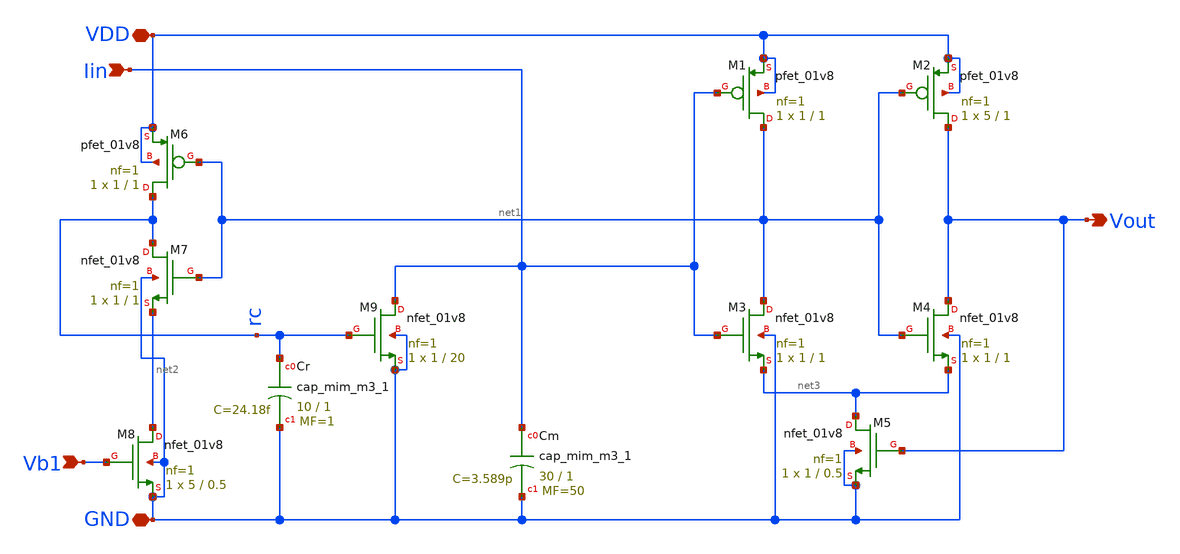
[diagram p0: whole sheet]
** sch_path: LIF_neuron/LIF_neuron_Vohra_CC.sch
**.subckt LIF_neuron_Vohra_CC GND Vb1 VDD Vout Iin
*.iopin GND
*.ipin Vb1
*.iopin VDD
*.opin Vout
*.ipin Iin
XM8 net2 Vb1 GND GND sky130_fd_pr__nfet_01v8 L=0.5 W=5 nf=1 ad='int((nf+1)/2) * W/nf * 0.29' as='int((nf+2)/2) * W/nf * 0.29'
+ pd='2*int((nf+1)/2) * (W/nf + 0.29)' ps='2*int((nf+2)/2) * (W/nf + 0.29)' nrd='0.29 / W' nrs='0.29 / W'
+ sa=0 sb=0 sd=0 mult=1 m=1
XM7 rc net1 net2 GND sky130_fd_pr__nfet_01v8 L=1 W=1 nf=1 ad='int((nf+1)/2) * W/nf * 0.29' as='int((nf+2)/2) * W/nf * 0.29'
+ pd='2*int((nf+1)/2) * (W/nf + 0.29)' ps='2*int((nf+2)/2) * (W/nf + 0.29)' nrd='0.29 / W' nrs='0.29 / W'
+ sa=0 sb=0 sd=0 mult=1 m=1
XM6 rc net1 VDD VDD sky130_fd_pr__pfet_01v8 L=1 W=1 nf=1 ad='int((nf+1)/2) * W/nf * 0.29' as='int((nf+2)/2) * W/nf * 0.29'
+ pd='2*int((nf+1)/2) * (W/nf + 0.29)' ps='2*int((nf+2)/2) * (W/nf + 0.29)' nrd='0.29 / W' nrs='0.29 / W'
+ sa=0 sb=0 sd=0 mult=1 m=1
XCr rc GND sky130_fd_pr__cap_mim_m3_1 W=10 L=1 MF=1 m=1
XM9 Iin rc GND GND sky130_fd_pr__nfet_01v8 L=20 W=1 nf=1 ad='int((nf+1)/2) * W/nf * 0.29' as='int((nf+2)/2) * W/nf * 0.29'
+ pd='2*int((nf+1)/2) * (W/nf + 0.29)' ps='2*int((nf+2)/2) * (W/nf + 0.29)' nrd='0.29 / W' nrs='0.29 / W'
+ sa=0 sb=0 sd=0 mult=1 m=1
XCm Iin GND sky130_fd_pr__cap_mim_m3_1 W=30 L=1 MF=50 m=50
XM5 net3 Vout GND GND sky130_fd_pr__nfet_01v8 L=0.5 W=1 nf=1 ad='int((nf+1)/2) * W/nf * 0.29' as='int((nf+2)/2) * W/nf * 0.29'
+ pd='2*int((nf+1)/2) * (W/nf + 0.29)' ps='2*int((nf+2)/2) * (W/nf + 0.29)' nrd='0.29 / W' nrs='0.29 / W'
+ sa=0 sb=0 sd=0 mult=1 m=1
XM3 net1 Iin net3 GND sky130_fd_pr__nfet_01v8 L=1 W=1 nf=1 ad='int((nf+1)/2) * W/nf * 0.29' as='int((nf+2)/2) * W/nf * 0.29'
+ pd='2*int((nf+1)/2) * (W/nf + 0.29)' ps='2*int((nf+2)/2) * (W/nf + 0.29)' nrd='0.29 / W' nrs='0.29 / W'
+ sa=0 sb=0 sd=0 mult=1 m=1
XM1 net1 Iin VDD VDD sky130_fd_pr__pfet_01v8 L=1 W=1 nf=1 ad='int((nf+1)/2) * W/nf * 0.29' as='int((nf+2)/2) * W/nf * 0.29'
+ pd='2*int((nf+1)/2) * (W/nf + 0.29)' ps='2*int((nf+2)/2) * (W/nf + 0.29)' nrd='0.29 / W' nrs='0.29 / W'
+ sa=0 sb=0 sd=0 mult=1 m=1
XM4 Vout net1 net3 GND sky130_fd_pr__nfet_01v8 L=1 W=1 nf=1 ad='int((nf+1)/2) * W/nf * 0.29' as='int((nf+2)/2) * W/nf * 0.29'
+ pd='2*int((nf+1)/2) * (W/nf + 0.29)' ps='2*int((nf+2)/2) * (W/nf + 0.29)' nrd='0.29 / W' nrs='0.29 / W'
+ sa=0 sb=0 sd=0 mult=1 m=1
XM2 Vout net1 VDD VDD sky130_fd_pr__pfet_01v8 L=1 W=5 nf=1 ad='int((nf+1)/2) * W/nf * 0.29' as='int((nf+2)/2) * W/nf * 0.29'
+ pd='2*int((nf+1)/2) * (W/nf + 0.29)' ps='2*int((nf+2)/2) * (W/nf + 0.29)' nrd='0.29 / W' nrs='0.29 / W'
+ sa=0 sb=0 sd=0 mult=1 m=1
**.ends
.end
